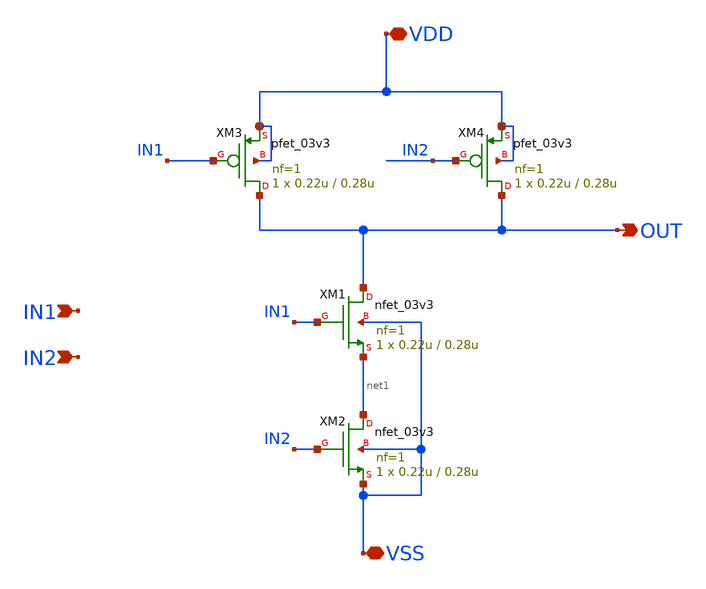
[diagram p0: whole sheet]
** sch_path: designs/libs/nand/nand.sch
**.subckt nand IN1 IN2 OUT VDD VSS
*.ipin IN1
*.ipin IN2
*.opin OUT
*.iopin VDD
*.iopin VSS
XM1 OUT IN1 net1 VSS nfet_03v3 L=0.28u W=0.22u nf=1 ad='int((nf+1)/2) * W/nf * 0.18u' as='int((nf+2)/2) * W/nf * 0.18u'
+ pd='2*int((nf+1)/2) * (W/nf + 0.18u)' ps='2*int((nf+2)/2) * (W/nf + 0.18u)' nrd='0.18u / W' nrs='0.18u / W'
+ sa=0 sb=0 sd=0 m=1
XM2 net1 IN2 VSS VSS nfet_03v3 L=0.28u W=0.22u nf=1 ad='int((nf+1)/2) * W/nf * 0.18u' as='int((nf+2)/2) * W/nf * 0.18u'
+ pd='2*int((nf+1)/2) * (W/nf + 0.18u)' ps='2*int((nf+2)/2) * (W/nf + 0.18u)' nrd='0.18u / W' nrs='0.18u / W'
+ sa=0 sb=0 sd=0 m=1
XM3 OUT IN1 VDD VDD pfet_03v3 L=0.28u W=0.22u nf=1 ad='int((nf+1)/2) * W/nf * 0.18u' as='int((nf+2)/2) * W/nf * 0.18u'
+ pd='2*int((nf+1)/2) * (W/nf + 0.18u)' ps='2*int((nf+2)/2) * (W/nf + 0.18u)' nrd='0.18u / W' nrs='0.18u / W'
+ sa=0 sb=0 sd=0 m=1
XM4 OUT IN2 VDD VDD pfet_03v3 L=0.28u W=0.22u nf=1 ad='int((nf+1)/2) * W/nf * 0.18u' as='int((nf+2)/2) * W/nf * 0.18u'
+ pd='2*int((nf+1)/2) * (W/nf + 0.18u)' ps='2*int((nf+2)/2) * (W/nf + 0.18u)' nrd='0.18u / W' nrs='0.18u / W'
+ sa=0 sb=0 sd=0 m=1
**.ends
.end
